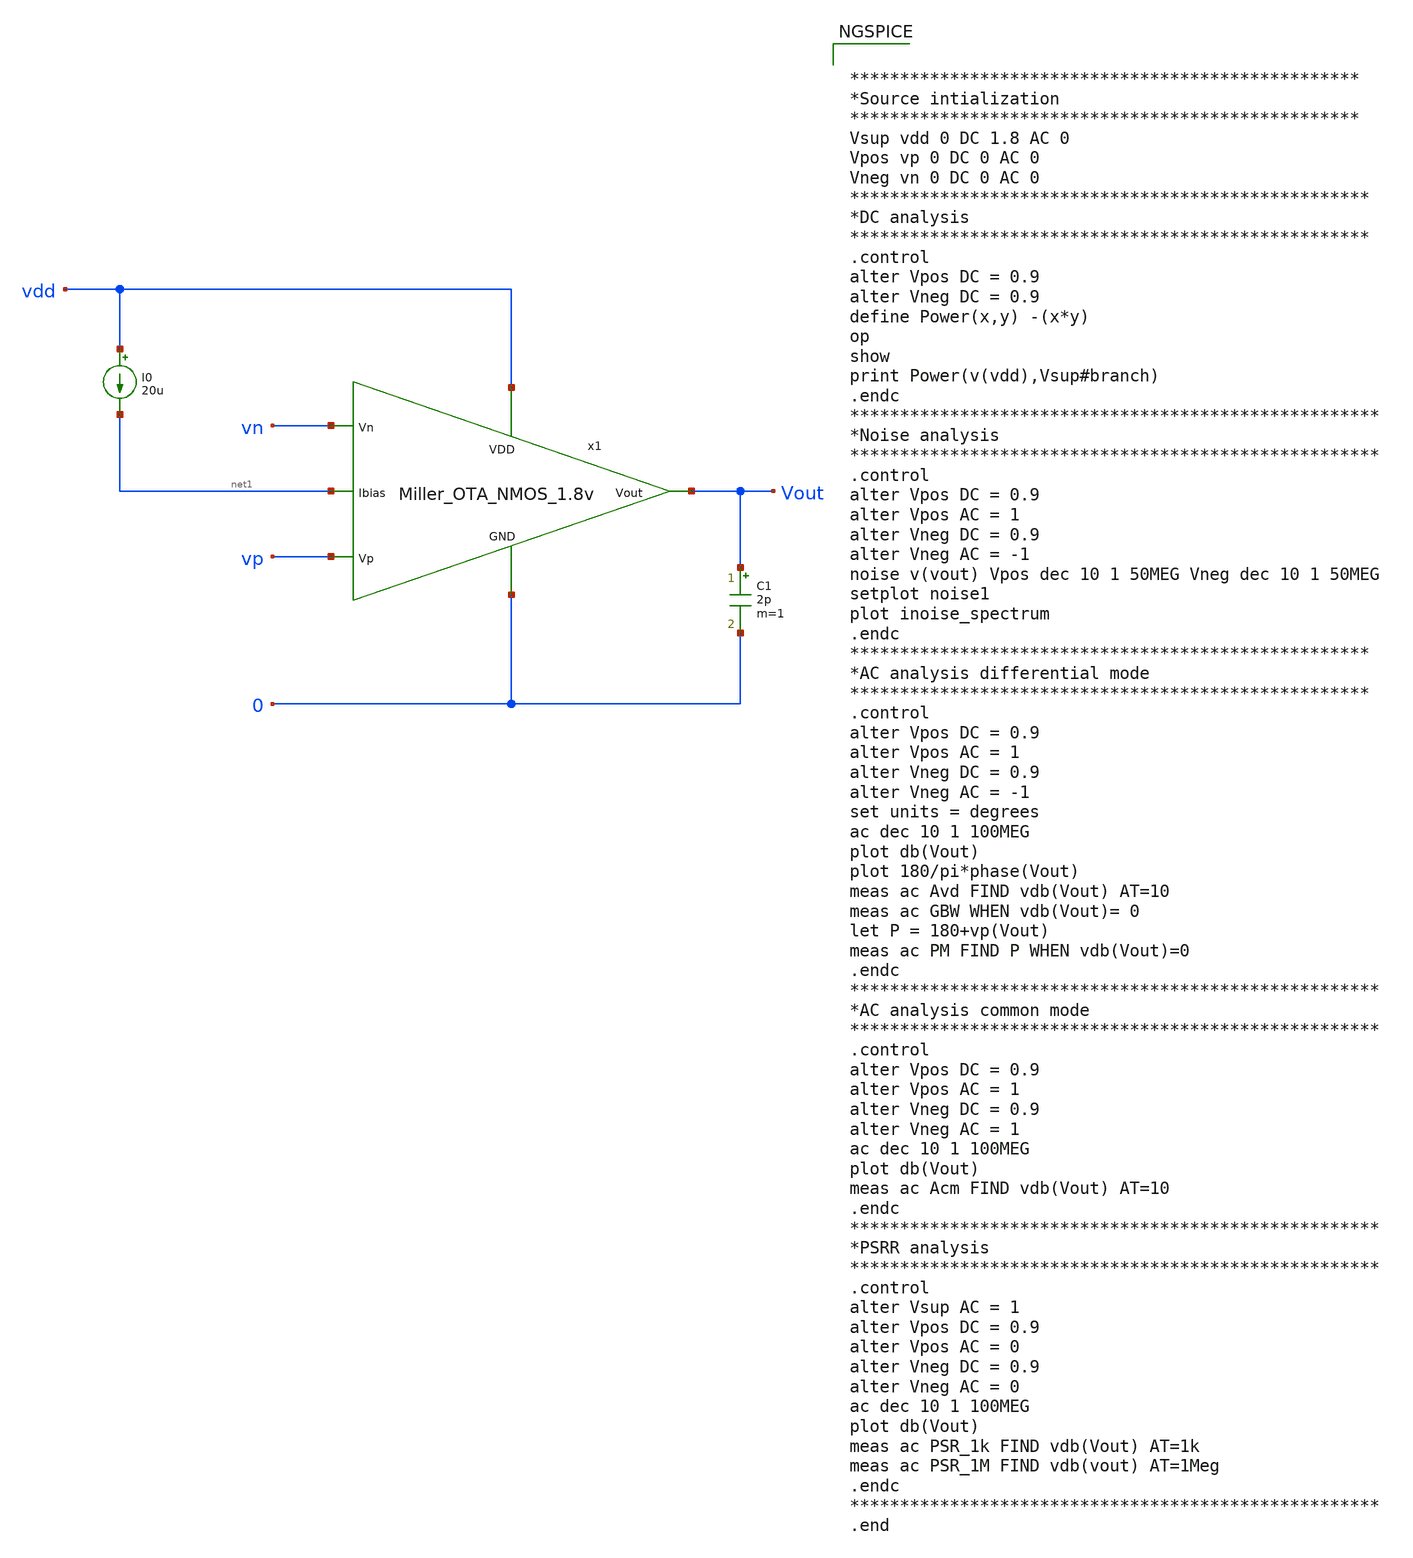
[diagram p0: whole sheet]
** sch_path: Analog_Blocks/OTA/Testbench/Miller_OTA_meas.sch
**.subckt Miller_OTA_meas
I0 vdd net1 20u
C1 Vout 0 2p m=1
x1 vdd vn vp Vout net1 0 Miller_OTA_NMOS_1.8v
**** begin user architecture code


***************************************************
*Source intialization
***************************************************
Vsup vdd 0 DC 1.8 AC 0
Vpos vp 0 DC 0 AC 0
Vneg vn 0 DC 0 AC 0
****************************************************
*DC analysis
****************************************************
.control
alter Vpos DC = 0.9
alter Vneg DC = 0.9
define Power(x,y) -(x*y)
op
show
print Power(v(vdd),Vsup#branch)
.endc
*****************************************************
*Noise analysis
*****************************************************
.control
alter Vpos DC = 0.9
alter Vpos AC = 1
alter Vneg DC = 0.9
alter Vneg AC = -1
noise v(vout) Vpos dec 10 1 50MEG Vneg dec 10 1 50MEG
setplot noise1
plot inoise_spectrum
.endc
****************************************************
*AC analysis differential mode
****************************************************
.control
alter Vpos DC = 0.9
alter Vpos AC = 1
alter Vneg DC = 0.9
alter Vneg AC = -1
set units = degrees
ac dec 10 1 100MEG
plot db(Vout)
plot 180/pi*phase(Vout)
meas ac Avd FIND vdb(Vout) AT=10
meas ac GBW WHEN vdb(Vout)= 0
let P = 180+vp(Vout)
meas ac PM FIND P WHEN vdb(Vout)=0
.endc
*****************************************************
*AC analysis common mode
*****************************************************
.control
alter Vpos DC = 0.9
alter Vpos AC = 1
alter Vneg DC = 0.9
alter Vneg AC = 1
ac dec 10 1 100MEG
plot db(Vout)
meas ac Acm FIND vdb(Vout) AT=10
.endc
*****************************************************
*PSRR analysis
*****************************************************
.control
alter Vsup AC = 1
alter Vpos DC = 0.9
alter Vpos AC = 0
alter Vneg DC = 0.9
alter Vneg AC = 0
ac dec 10 1 100MEG
plot db(Vout)
meas ac PSR_1k FIND vdb(Vout) AT=1k
meas ac PSR_1M FIND vdb(vout) AT=1Meg
.endc
*****************************************************
.end


**** end user architecture code
**.ends
.end
